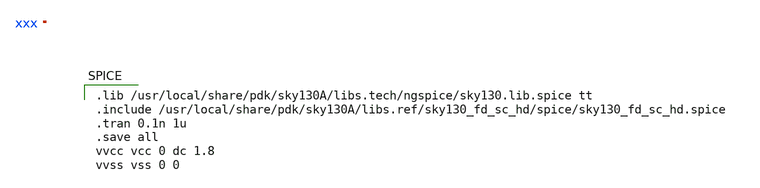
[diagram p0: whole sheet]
** sch_path: sky130-sim/buffer_chain/buffer_chain.sch
**.subckt buffer_chain
**** begin user architecture code

.lib /usr/local/share/pdk/sky130A/libs.tech/ngspice/sky130.lib.spice tt
.include /usr/local/share/pdk/sky130A/libs.ref/sky130_fd_sc_hd/spice/sky130_fd_sc_hd.spice
.tran 0.1n 1u
.save all
vvcc vcc 0 dc 1.8
vvss vss 0 0


**** end user architecture code
**.ends
.end
